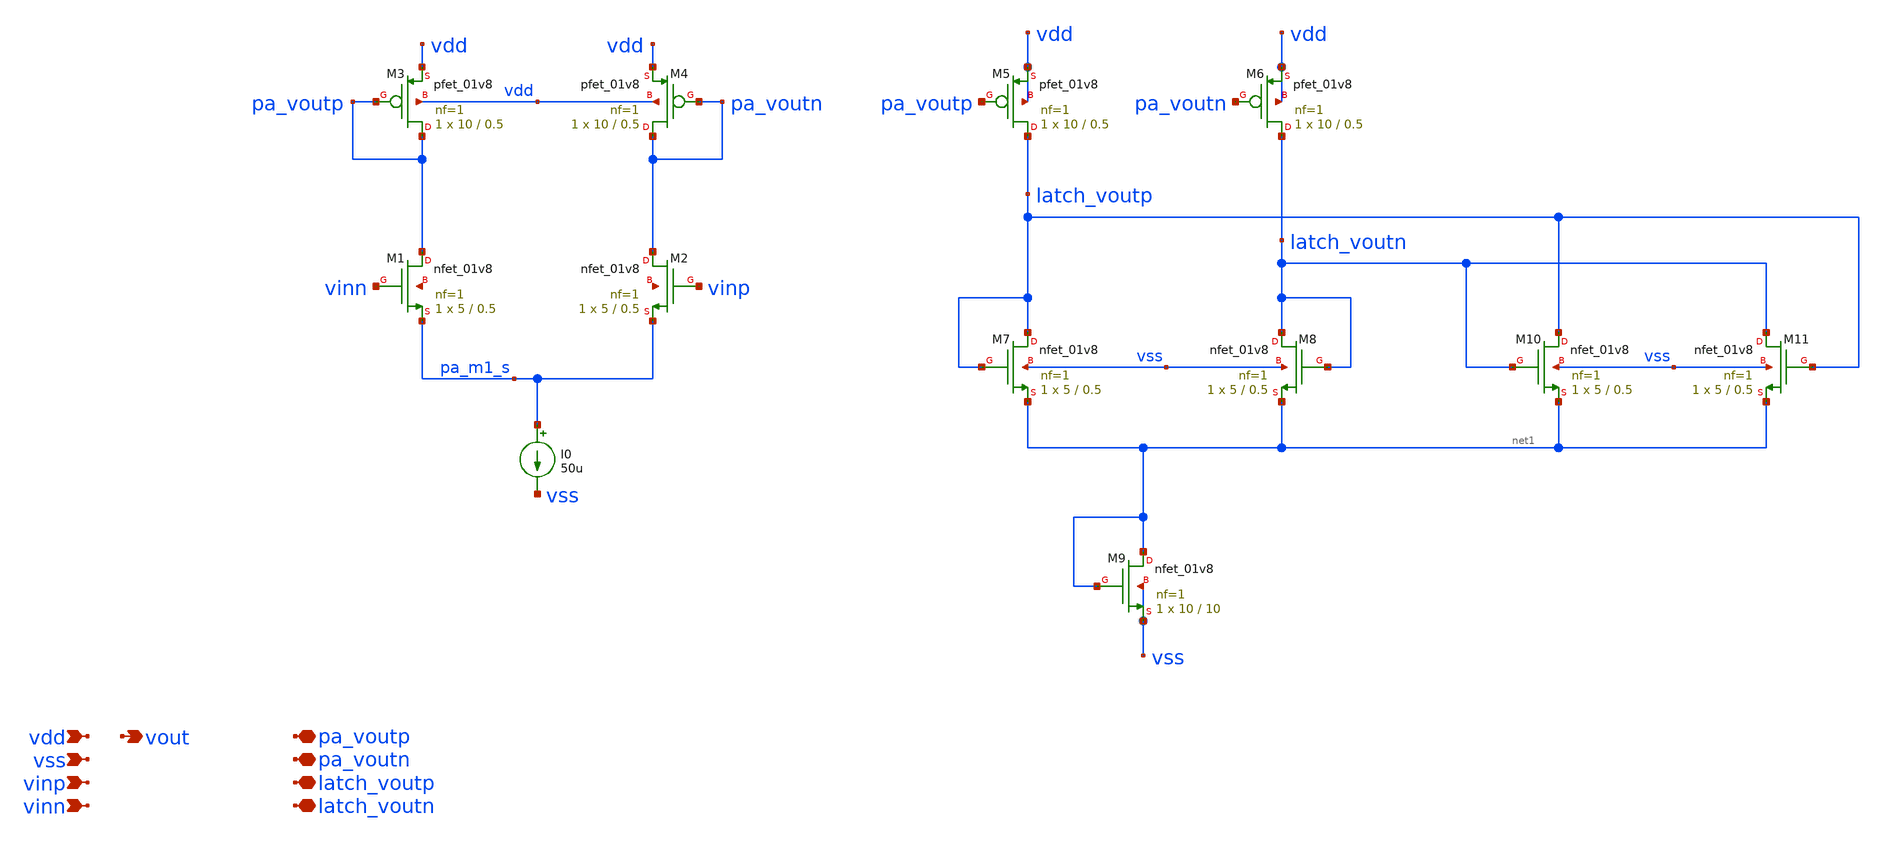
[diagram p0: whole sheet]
** sch_path: schematics/comp_pa_latch.sch
**.subckt comp_pa_latch vdd vout vss vinp vinn pa_voutp pa_voutn latch_voutp latch_voutn
*.ipin vdd
*.opin vout
*.ipin vss
*.ipin vinp
*.ipin vinn
*.iopin pa_voutp
*.iopin pa_voutn
*.iopin latch_voutp
*.iopin latch_voutn
I0 pa_m1_s vss 50u
XM1 pa_voutp vinn pa_m1_s net2 sky130_fd_pr__nfet_01v8 L=0.5 W=5 nf=1 ad='int((1 + 1)/2) * 5 / 1 * 0.29'
+ as='int((1 + 2)/2) * 5 / 1 * 0.29' pd='2*int((1 + 1)/2) * (5 / 1 + 0.29)' ps='2*int((1 + 2)/2) * (5 / 1 + 0.29)'
+ nrd='0.29 / 5 ' nrs='0.29 / 5 ' sa=0 sb=0 sd=0 mult=1 m=1
XM2 pa_voutn vinp pa_m1_s net3 sky130_fd_pr__nfet_01v8 L=0.5 W=5 nf=1 ad='int((1 + 1)/2) * 5 / 1 * 0.29'
+ as='int((1 + 2)/2) * 5 / 1 * 0.29' pd='2*int((1 + 1)/2) * (5 / 1 + 0.29)' ps='2*int((1 + 2)/2) * (5 / 1 + 0.29)'
+ nrd='0.29 / 5 ' nrs='0.29 / 5 ' sa=0 sb=0 sd=0 mult=1 m=1
XM3 pa_voutp pa_voutp vdd vdd sky130_fd_pr__pfet_01v8 L=0.5 W=10 nf=1 ad='int((1 + 1)/2) * 10 / 1 * 0.29'
+ as='int((1 + 2)/2) * 10 / 1 * 0.29' pd='2*int((1 + 1)/2) * (10 / 1 + 0.29)' ps='2*int((1 + 2)/2) * (10 / 1 + 0.29)'
+ nrd='0.29 / 10 ' nrs='0.29 / 10 ' sa=0 sb=0 sd=0 mult=1 m=1
XM4 pa_voutn pa_voutn vdd vdd sky130_fd_pr__pfet_01v8 L=0.5 W=10 nf=1 ad='int((1 + 1)/2) * 10 / 1 * 0.29'
+ as='int((1 + 2)/2) * 10 / 1 * 0.29' pd='2*int((1 + 1)/2) * (10 / 1 + 0.29)' ps='2*int((1 + 2)/2) * (10 / 1 + 0.29)'
+ nrd='0.29 / 10 ' nrs='0.29 / 10 ' sa=0 sb=0 sd=0 mult=1 m=1
XM5 latch_voutp pa_voutp vdd vdd sky130_fd_pr__pfet_01v8 L=0.5 W=10 nf=1 ad='int((1 + 1)/2) * 10 / 1 * 0.29'
+ as='int((1 + 2)/2) * 10 / 1 * 0.29' pd='2*int((1 + 1)/2) * (10 / 1 + 0.29)' ps='2*int((1 + 2)/2) * (10 / 1 + 0.29)'
+ nrd='0.29 / 10 ' nrs='0.29 / 10 ' sa=0 sb=0 sd=0 mult=1 m=1
XM6 latch_voutn pa_voutn vdd vdd sky130_fd_pr__pfet_01v8 L=0.5 W=10 nf=1 ad='int((1 + 1)/2) * 10 / 1 * 0.29'
+ as='int((1 + 2)/2) * 10 / 1 * 0.29' pd='2*int((1 + 1)/2) * (10 / 1 + 0.29)' ps='2*int((1 + 2)/2) * (10 / 1 + 0.29)'
+ nrd='0.29 / 10 ' nrs='0.29 / 10 ' sa=0 sb=0 sd=0 mult=1 m=1
XM7 latch_voutp latch_voutp net1 vss sky130_fd_pr__nfet_01v8 L=0.5 W=5 nf=1 ad='int((1 + 1)/2) * 5 / 1 * 0.29'
+ as='int((1 + 2)/2) * 5 / 1 * 0.29' pd='2*int((1 + 1)/2) * (5 / 1 + 0.29)' ps='2*int((1 + 2)/2) * (5 / 1 + 0.29)'
+ nrd='0.29 / 5 ' nrs='0.29 / 5 ' sa=0 sb=0 sd=0 mult=1 m=1
XM8 latch_voutn latch_voutn net1 vss sky130_fd_pr__nfet_01v8 L=0.5 W=5 nf=1 ad='int((1 + 1)/2) * 5 / 1 * 0.29'
+ as='int((1 + 2)/2) * 5 / 1 * 0.29' pd='2*int((1 + 1)/2) * (5 / 1 + 0.29)' ps='2*int((1 + 2)/2) * (5 / 1 + 0.29)'
+ nrd='0.29 / 5 ' nrs='0.29 / 5 ' sa=0 sb=0 sd=0 mult=1 m=1
XM9 net1 net1 vss vss sky130_fd_pr__nfet_01v8 L=10 W=10 nf=1 ad='int((1 + 1)/2) * 10 / 1 * 0.29' as='int((1 + 2)/2) * 10 / 1 * 0.29'
+ pd='2*int((1 + 1)/2) * (10 / 1 + 0.29)' ps='2*int((1 + 2)/2) * (10 / 1 + 0.29)' nrd='0.29 / 10 ' nrs='0.29 / 10 '
+ sa=0 sb=0 sd=0 mult=1 m=1
XM10 latch_voutp latch_voutn net1 vss sky130_fd_pr__nfet_01v8 L=0.5 W=5 nf=1 ad='int((1 + 1)/2) * 5 / 1 * 0.29'
+ as='int((1 + 2)/2) * 5 / 1 * 0.29' pd='2*int((1 + 1)/2) * (5 / 1 + 0.29)' ps='2*int((1 + 2)/2) * (5 / 1 + 0.29)'
+ nrd='0.29 / 5 ' nrs='0.29 / 5 ' sa=0 sb=0 sd=0 mult=1 m=1
XM11 latch_voutn latch_voutp net1 vss sky130_fd_pr__nfet_01v8 L=0.5 W=5 nf=1 ad='int((1 + 1)/2) * 5 / 1 * 0.29'
+ as='int((1 + 2)/2) * 5 / 1 * 0.29' pd='2*int((1 + 1)/2) * (5 / 1 + 0.29)' ps='2*int((1 + 2)/2) * (5 / 1 + 0.29)'
+ nrd='0.29 / 5 ' nrs='0.29 / 5 ' sa=0 sb=0 sd=0 mult=1 m=1
**.ends
.end
